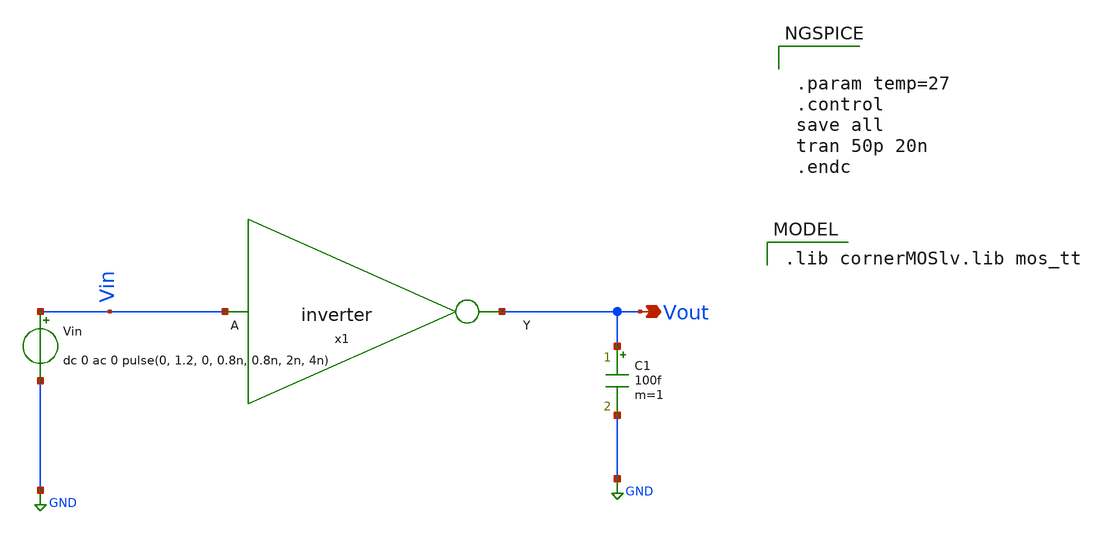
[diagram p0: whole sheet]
** sch_path: Team Designs/Team 1 Design/design_data/xschem/Inverter/inverter_tb.sch
**.subckt inverter_tb Vout
*.opin Vout
Vin Vin GND dc 0 ac 0 pulse(0, 1.2, 0, 0.8n, 0.8n, 2n, 4n)
C1 Vout GND 100f m=1
x1 Vout Vin inverter
**** begin user architecture code
 .lib cornerMOSlv.lib mos_tt



.param temp=27
.control
save all
tran 50p 20n
.endc


**** end user architecture code
**.ends
.GLOBAL GND
.end
